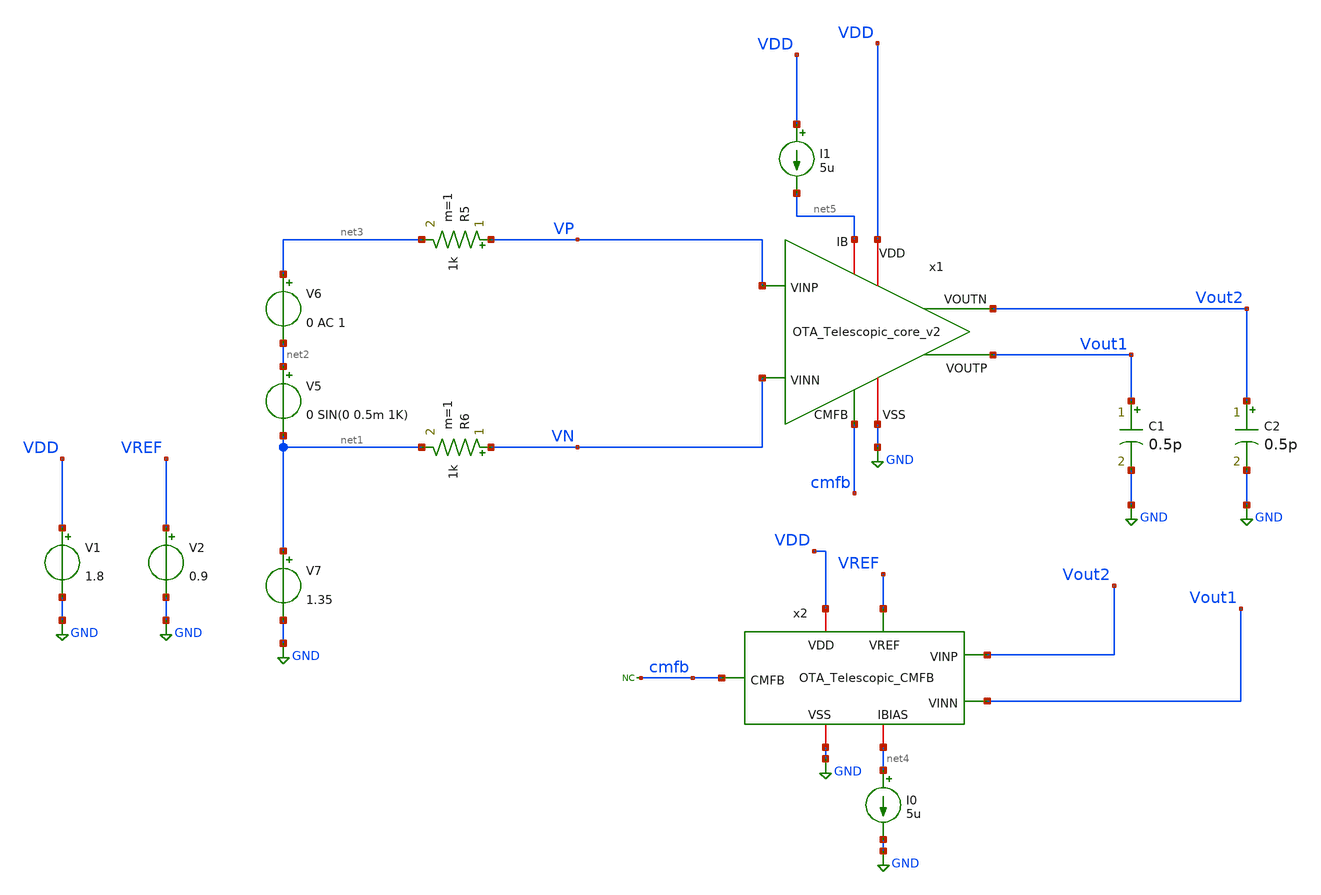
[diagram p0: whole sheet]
** sch_path: Differential_OTA_Telescopic_IHP/OTA_Telescopic_CMFB_TB2.sch
**.subckt OTA_Telescopic_CMFB_TB2
V6 net3 net2 0 AC 1
V7 net1 GND 1.35
V5 net2 net1 0 SIN(0 0.5m 1K)
V1 VDD GND 1.8
V2 VREF GND 0.9
C1 Vout1 GND 0.5p m=1
C2 Vout2 GND 0.5p m=1
I0 net4 GND 5u
x2 VDD VREF Vout1 Vout2 net4 cmfb GND OTA_Telescopic_CMFB
R5 VP net3 1k m=1
R6 VN net1 1k m=1
* noconn cmfb
I1 VDD net5 5u
x1 VDD cmfb Vout1 Vout2 VP VN GND net5 OTA_Telescopic_core_v2
**** begin user architecture code

** opencircuitdesign pdks install
.lib $::SKYWATER_MODELS/sky130.lib.spice tt




.control
save all
 set color0 = white

* AC simulation
ac dec 10 1 1T
let Av = db(v(Vout1)-v(Vout2))
meas ac Ao MAX Av
let ABW = Ao-3
meas ac BW WHEN Av=ABW
meas ac UGBW WHEN Av=0
let phase_vec = 180/pi*cph(v(Vout1)-v(Vout2))

* Phase margin (PM)
meas ac phase FIND phase_vec WHEN frequency=UGBW
let PM = phase+180
print PM

* Gain margin (GM)
meas ac freq180 FIND frequency WHEN phase_vec=-180
meas ac gain FIND Av WHEN frequency=freq180
let GM = 0-gain
print GM
plot Av
plot phase_vec

write AC_OL.raw


*DC simulation

op
let vout_dc = v(Vout1)
print vout_dc
write OTA_Telescopic_TB2.raw

.endc




.op

.save all
*OTA
.save @m.x1.xm1.msky130_fd_pr__nfet_01v8_lvt[id]
.save @m.x1.xm1.msky130_fd_pr__nfet_01v8_lvt[gm]
.save @m.x1.xm2.msky130_fd_pr__nfet_01v8_lvt[id]
.save @m.x1.xm2.msky130_fd_pr__nfet_01v8_lvt[gm]

.save @m.x1.xm9.msky130_fd_pr__pfet_01v8_lvt[id]
.save @m.x1.xm9.msky130_fd_pr__pfet_01v8_lvt[gm]
.save @m.x1.xm10.msky130_fd_pr__pfet_01v8_lvt[id]
.save @m.x1.xm10.msky130_fd_pr__pfet_01v8_lvt[gm]

.save @m.x1.xm0.msky130_fd_pr__nfet_01v8_lvt[id]

.save @m.x1.xm1.msky130_fd_pr__nfet_01v8_lvt[vdssat]


.save @m.x1.xm13.msky130_fd_pr__nfet_01v8_lvt[id]
.save @m.x1.xm14.msky130_fd_pr__nfet_01v8_lvt[id]
.save @m.x1.xm15.msky130_fd_pr__pfet_01v8_lvt[id]
.save @m.x1.xm16.msky130_fd_pr__nfet_01v8_lvt[id]
.save @m.x1.xm17.msky130_fd_pr__nfet_01v8_lvt[id]

.save @m.x1.xm18.msky130_fd_pr__pfet_01v8_lvt[id]
.save @m.x1.xm19.msky130_fd_pr__nfet_01v8_lvt[id]

*CMFB
.save @m.x2.xm0.msky130_fd_pr__pfet_01v8_lvt[id]
.save @m.x2.xm1.msky130_fd_pr__pfet_01v8_lvt[id]
.save @m.x2.xm1.msky130_fd_pr__pfet_01v8_lvt[gm]
.save @m.x2.xm2.msky130_fd_pr__pfet_01v8_lvt[id]
.save @m.x2.xm2.msky130_fd_pr__pfet_01v8_lvt[gm]
.save @m.x2.xm3.msky130_fd_pr__pfet_01v8_lvt[id]
.save @m.x2.xm3.msky130_fd_pr__pfet_01v8_lvt[gm]
.save @m.x2.xm4.msky130_fd_pr__pfet_01v8_lvt[id]
.save @m.x2.xm4.msky130_fd_pr__pfet_01v8_lvt[gm]
.save @m.x2.xm5.msky130_fd_pr__pfet_01v8_lvt[id]
.save @m.x2.xm5.msky130_fd_pr__pfet_01v8_lvt[gm]
.save @m.x2.xm6.msky130_fd_pr__pfet_01v8_lvt[id]
.save @m.x2.xm6.msky130_fd_pr__pfet_01v8_lvt[gm]

.save @m.x2.xm7.msky130_fd_pr__nfet_01v8_lvt[id]
.save @m.x2.xm7.msky130_fd_pr__nfet_01v8_lvt[gm]
.save @m.x2.xm8.msky130_fd_pr__nfet_01v8_lvt[id]
.save @m.x2.xm8.msky130_fd_pr__nfet_01v8_lvt[gm]



.control

let vdssat_M1 = @m.x1.xm1.msky130_fd_pr__nfet_01v8_lvt[vdsat]
let vdssat_M3 = @m.x1.xm3.msky130_fd_pr__nfet_01v8_lvt[vdsat]
let vdssat_M5 = @m.x1.xm5.msky130_fd_pr__pfet_01v8_lvt[vdsat]
let vdssat_M7 = @m.x1.xm7.msky130_fd_pr__pfet_01v8_lvt[vdsat]
let vdssat_M0 = @m.x1.xm0.msky130_fd_pr__nfet_01v8_lvt[vdsat]

print vdssat_M1
print vdssat_M3
print vdssat_M5
print vdssat_M7
print vdssat_M0

let ro_M1 = 1/@m.x1.xm1.msky130_fd_pr__nfet_01v8_lvt[gds]
let ro_M3 = 1/@m.x1.xm3.msky130_fd_pr__nfet_01v8_lvt[gds]
let ro_M5 = 1/@m.x1.xm5.msky130_fd_pr__pfet_01v8_lvt[gds]
let ro_M7 = 1/@m.x1.xm7.msky130_fd_pr__pfet_01v8_lvt[gds]
let ro_M0 = 1/@m.x1.xm0.msky130_fd_pr__nfet_01v8_lvt[gds]

print ro_M1
print ro_M3
print ro_M5
print ro_M7
print ro_M0

let gm_M1 = @m.x1.xm1.msky130_fd_pr__nfet_01v8_lvt[gm]
let gm_M3 = @m.x1.xm3.msky130_fd_pr__nfet_01v8_lvt[gm]
let gm_M5 = @m.x1.xm5.msky130_fd_pr__pfet_01v8_lvt[gm]
let gm_M7 = @m.x1.xm7.msky130_fd_pr__pfet_01v8_lvt[gm]
let gm_M0 = @m.x1.xm0.msky130_fd_pr__nfet_01v8_lvt[gm]

print gm_M1
print gm_M3
print gm_M5
print gm_M7
print gm_M0

let gmb_M3 = @m.x1.xm3.msky130_fd_pr__nfet_01v8_lvt[gmbs]
let gmb_M5 = @m.x1.xm5.msky130_fd_pr__pfet_01v8_lvt[gmbs]

print gmb_M3
print gmb_M5


*CMFB

let x2_vdssat_M0 = @m.x2.xm0.msky130_fd_pr__pfet_01v8_lvt[vdsat]
let x2_vth_M0 = @m.x2.xm0.msky130_fd_pr__pfet_01v8_lvt[vth]

print x2_vdssat_M0
print x2_vth_M0

.endc



**** end user architecture code
**.ends

* expanding   symbol:  OTA_Telescopic_CMFB.sym # of pins=7
** sym_path: Differential_OTA_Telescopic_IHP/OTA_Telescopic_CMFB.sym
** sch_path: Differential_OTA_Telescopic_IHP/OTA_Telescopic_CMFB.sch
.subckt OTA_Telescopic_CMFB VDD VREF VINN VINP IBIAS CMFB VSS
*.iopin VDD
*.iopin VSS
*.opin CMFB
*.ipin VREF
*.iopin IBIAS
*.ipin VINP
*.ipin VINN
XM0 IBIAS IBIAS VDD VDD sky130_fd_pr__pfet_01v8_lvt L=0.85 W=15 nf=1 ad='int((nf+1)/2) * W/nf * 0.29'
+ as='int((nf+2)/2) * W/nf * 0.29' pd='2*int((nf+1)/2) * (W/nf + 0.29)' ps='2*int((nf+2)/2) * (W/nf + 0.29)'
+ nrd='0.29 / W' nrs='0.29 / W' sa=0 sb=0 sd=0 mult=1 m=1
XM7 net1 net1 VSS VSS sky130_fd_pr__nfet_01v8_lvt L=0.8 W=6 nf=1 ad='int((nf+1)/2) * W/nf * 0.29' as='int((nf+2)/2) * W/nf * 0.29'
+ pd='2*int((nf+1)/2) * (W/nf + 0.29)' ps='2*int((nf+2)/2) * (W/nf + 0.29)' nrd='0.29 / W' nrs='0.29 / W'
+ sa=0 sb=0 sd=0 mult=2 m=2
XM4 net1 VREF V1 VDD sky130_fd_pr__pfet_01v8_lvt L=0.35 W=20 nf=1 ad='int((nf+1)/2) * W/nf * 0.29' as='int((nf+2)/2) * W/nf * 0.29'
+ pd='2*int((nf+1)/2) * (W/nf + 0.29)' ps='2*int((nf+2)/2) * (W/nf + 0.29)' nrd='0.29 / W' nrs='0.29 / W'
+ sa=0 sb=0 sd=0 mult=1 m=1
XM5 net1 VREF V2 VDD sky130_fd_pr__pfet_01v8_lvt L=0.35 W=20 nf=1 ad='int((nf+1)/2) * W/nf * 0.29' as='int((nf+2)/2) * W/nf * 0.29'
+ pd='2*int((nf+1)/2) * (W/nf + 0.29)' ps='2*int((nf+2)/2) * (W/nf + 0.29)' nrd='0.29 / W' nrs='0.29 / W'
+ sa=0 sb=0 sd=0 mult=1 m=1
XM3 CMFB VINP V1 VDD sky130_fd_pr__pfet_01v8_lvt L=0.35 W=20 nf=1 ad='int((nf+1)/2) * W/nf * 0.29' as='int((nf+2)/2) * W/nf * 0.29'
+ pd='2*int((nf+1)/2) * (W/nf + 0.29)' ps='2*int((nf+2)/2) * (W/nf + 0.29)' nrd='0.29 / W' nrs='0.29 / W'
+ sa=0 sb=0 sd=0 mult=1 m=1
XM6 CMFB VINN V2 VDD sky130_fd_pr__pfet_01v8_lvt L=0.35 W=20 nf=1 ad='int((nf+1)/2) * W/nf * 0.29' as='int((nf+2)/2) * W/nf * 0.29'
+ pd='2*int((nf+1)/2) * (W/nf + 0.29)' ps='2*int((nf+2)/2) * (W/nf + 0.29)' nrd='0.29 / W' nrs='0.29 / W'
+ sa=0 sb=0 sd=0 mult=1 m=1
XM1 V1 IBIAS VDD VDD sky130_fd_pr__pfet_01v8_lvt L=0.85 W=15 nf=1 ad='int((nf+1)/2) * W/nf * 0.29' as='int((nf+2)/2) * W/nf * 0.29'
+ pd='2*int((nf+1)/2) * (W/nf + 0.29)' ps='2*int((nf+2)/2) * (W/nf + 0.29)' nrd='0.29 / W' nrs='0.29 / W'
+ sa=0 sb=0 sd=0 mult=1 m=1
XM2 V2 IBIAS VDD VDD sky130_fd_pr__pfet_01v8_lvt L=0.85 W=15 nf=1 ad='int((nf+1)/2) * W/nf * 0.29' as='int((nf+2)/2) * W/nf * 0.29'
+ pd='2*int((nf+1)/2) * (W/nf + 0.29)' ps='2*int((nf+2)/2) * (W/nf + 0.29)' nrd='0.29 / W' nrs='0.29 / W'
+ sa=0 sb=0 sd=0 mult=1 m=1
XM8 CMFB CMFB VSS VSS sky130_fd_pr__nfet_01v8_lvt L=0.8 W=6 nf=1 ad='int((nf+1)/2) * W/nf * 0.29' as='int((nf+2)/2) * W/nf * 0.29'
+ pd='2*int((nf+1)/2) * (W/nf + 0.29)' ps='2*int((nf+2)/2) * (W/nf + 0.29)' nrd='0.29 / W' nrs='0.29 / W'
+ sa=0 sb=0 sd=0 mult=2 m=2
.ends


* expanding   symbol:  OTA_Telescopic_core_v2.sym # of pins=8
** sym_path: OTA_Telescopic_core_v2.sym
** sch_path: OTA_Telescopic_core_v2.sch
.subckt OTA_Telescopic_core_v2 VDD CMFB VOUTP VOUTN VINP VINN VSS IB
*.iopin VDD
*.iopin VSS
*.ipin VINP
*.ipin VINN
*.opin VOUTN
*.opin VOUTP
*.ipin CMFB
*.iopin IB
V2 VB2 VSS 1.5
V3 VB3 VSS 0.7
V4 VB4 VSS 0.49409
V1 VB5 VSS 1.12
* noconn VB2
* noconn VB3
* noconn VB4
* noconn VB5
V5 VB VSS 0.90204
* noconn VB
R1 net1 VOUTP 190 m=1
R2 VOUTN net2 190 m=1
C1 Vo1 net1 0.63p m=1
C2 Vo2 net2 0.63p m=1
XM15 VB55 VB55 VDD VDD sg13_lv_pmos w=1.45u l=0.35u ng=1 m=6 mm_ok=1
XM17 VB33 VB33 VDD VDD sg13_lv_pmos w=2.05u l=0.35u ng=1 m=1 mm_ok=1
XM18 VB22 VB33 VDD VDD sg13_lv_pmos w=2.05u l=0.35u ng=1 m=1 mm_ok=1
XM9 VOUTP Vo1 VDD VDD sg13_lv_pmos w=1.37u l=0.35u ng=1 m=200 mm_ok=1
XM7 Vx1 VB55 VDD VDD sg13_lv_pmos w=6.85u l=0.7u ng=1 m=30 mm_ok=1
XM5 Vo1 VB33 Vx1 VDD sg13_lv_pmos w=4.05u l=0.5u ng=1 m=30 mm_ok=1
XM8 Vx2 VB55 VDD VDD sg13_lv_pmos w=6.85u l=0.7u ng=1 m=30 mm_ok=1
XM6 Vo2 VB33 Vx2 VDD sg13_lv_pmos w=4.05u l=0.5u ng=1 m=30 mm_ok=1
XM10 VOUTN Vo2 VDD VDD sg13_lv_pmos w=1.37u l=0.35u ng=1 m=200 mm_ok=1
XM13 IB IB VSS VSS sg13_lv_nmos w=4.8u l=1.06u ng=1 m=1 mm_ok=1
XM14 VB55 IB VSS VSS sg13_lv_nmos w=4.8u l=1.06u ng=1 m=1 mm_ok=1
XM16 VB33 IB VSS VSS sg13_lv_nmos w=4.8u l=1.06u ng=1 m=1 mm_ok=1
XM19 VB22 VB22 VSS VSS sg13_lv_nmos w=0.5u l=0.8u ng=1 m=1 mm_ok=1
XM11 VOUTP IB VSS VSS sg13_lv_nmos w=4.8u l=1.06u ng=1 m=55 mm_ok=1
XM0 P CMFB VSS VSS sg13_lv_nmos w=30u l=0.3u ng=9 m=32 mm_ok=1
XM3 Vo1 VB22 Vy1 VSS sg13_lv_nmos w=1.9u l=0.16u ng=1 m=30 mm_ok=1
XM1 Vy1 VINP P VSS sg13_lv_nmos w=1.1u l=0.15u ng=1 m=30 mm_ok=1
XM4 Vo2 VB22 Vy2 VSS sg13_lv_nmos w=1.9u l=0.16u ng=1 m=30 mm_ok=1
XM2 Vy2 VINN P VSS sg13_lv_nmos w=1.1u l=0.15u ng=1 m=30 mm_ok=1
XM12 VOUTN IB VSS VSS sg13_lv_nmos w=4.8u l=1.06u ng=1 m=55 mm_ok=1
.ends

.GLOBAL GND
.end
